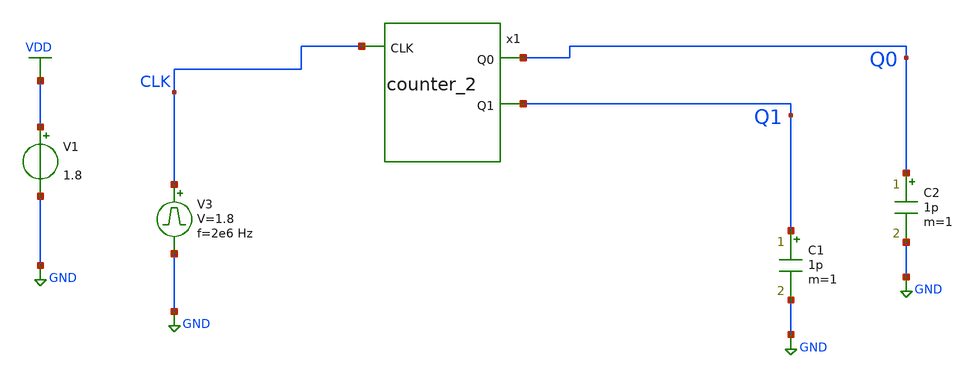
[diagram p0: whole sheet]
** sch_path: circuits/xschem/counter_2_tb.sch
**.subckt counter_2_tb
V1 VDD GND 1.8
V3 CLK GND pulse 0 1.8 '0.495/ 2e6 ' '0.01/2e6 ' '0.01/2e6 ' '0.49/2e6 ' '1/2e6 '
C2 Q0 GND 1p m=1
C1 Q1 GND 1p m=1
x1 Q0 Q1 CLK counter_2
**** begin user architecture code


.control
save all
tran 1n 4u
plot V(CLK) V(Q0)+2 V(Q1)+4
.endc



** opencircuitdesign pdks install
.lib $::SKYWATER_MODELS/sky130.lib.spice tt


**** end user architecture code
**.ends
.GLOBAL VDD
.GLOBAL GND
.end
